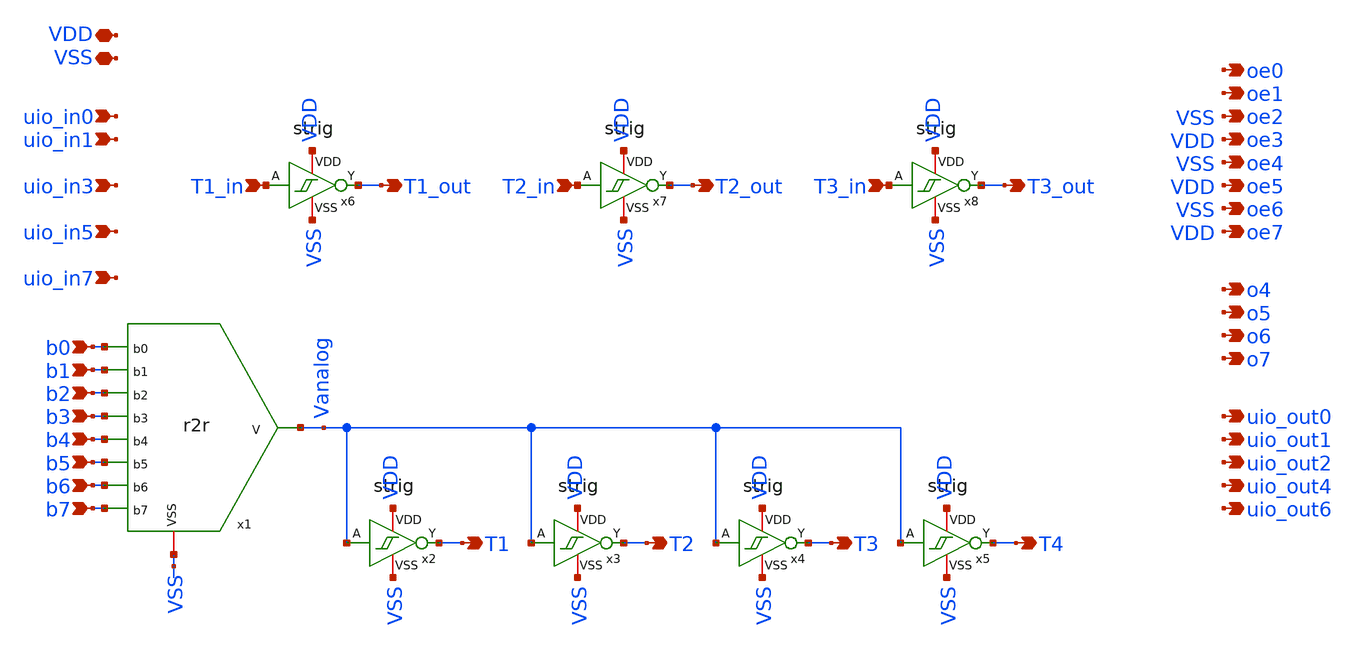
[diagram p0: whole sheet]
** sch_path: xschem/tt_um_mixer.sch
**.subckt tt_um_mixer b0 b1 b2 b3 b4 b5 b6 b7 VSS VDD T1 T2 T3 T4 T1_out T1_in T2_out T2_in T3_out
*+ T3_in oe0 oe1 oe2 oe3 oe4 oe5 oe6 oe7 uio_in0 uio_in1 uio_in3 uio_in5 uio_in7 o4 o5 o6 o7 uio_out0
*+ uio_out1 uio_out2 uio_out4 uio_out6
*.ipin b0
*.ipin b1
*.ipin b2
*.ipin b3
*.ipin b4
*.ipin b5
*.ipin b6
*.ipin b7
*.iopin VSS
*.iopin VDD
*.opin T1
*.opin T2
*.opin T3
*.opin T4
*.opin T1_out
*.ipin T1_in
*.opin T2_out
*.ipin T2_in
*.opin T3_out
*.ipin T3_in
*.opin oe0
*.opin oe1
*.opin oe2
*.opin oe3
*.opin oe4
*.opin oe5
*.opin oe6
*.opin oe7
*.ipin uio_in0
*.ipin uio_in1
*.ipin uio_in3
*.ipin uio_in5
*.ipin uio_in7
*.opin o4
*.opin o5
*.opin o6
*.opin o7
*.opin uio_out0
*.opin uio_out1
*.opin uio_out2
*.opin uio_out4
*.opin uio_out6
x2 VDD Vanalog T1 VSS strig WN1=.6u WN2=.6u WN3=.6u WP1=.6u WP2=.6u WP3=.6u
x1 b3 b1 b2 b0 b4 b5 b6 b7 Vanalog VSS r2r
x3 VDD Vanalog T2 VSS strig WN1=1.2u WN2=1.2u WN3=.6u WP1=1.2u WP2=1.2u WP3=.6u
x4 VDD Vanalog T3 VSS strig WN1=2.4u WN2=2.4u WN3=.6u WP1=2.4u WP2=2.4u WP3=.6u
x5 VDD Vanalog T4 VSS strig WN1=4.8u WN2=4.8u WN3=.6u WP1=4.8u WP2=4.8u WP3=.6u
x6 VDD T1_in T1_out VSS strig WN1=.6u WN2=.6u WN3=.6u WP1=.6u WP2=.6u WP3=.6u
x7 VDD T2_in T2_out VSS strig WN1=.6u WN2=.6u WN3=.6u WP1=.6u WP2=.6u WP3=.6u
x8 VDD T3_in T3_out VSS strig WN1=.6u WN2=.6u WN3=.6u WP1=.6u WP2=.6u WP3=.6u
**.ends

* expanding   symbol:  strig.sym # of pins=4
** sym_path: xschem/strig.sym
** sch_path: xschem/strig.sch
.subckt strig VDD A Y VSS  WN1=.15u WN2=.15u WN3=.15u WP1=.15u WP2=.15u WP3=.15u
*.iopin VDD
*.iopin VSS
*.ipin A
*.opin Y
XM1 net1 A VSS VSS sg13_lv_nmos w=WN1 l=0.13u ng=1 m=1 mm_ok=1
XM2 Y A net1 VSS sg13_lv_nmos w=WN2 l=0.13u ng=1 m=1 mm_ok=1
XM3 VDD Y net1 VSS sg13_lv_nmos w=WN3 l=0.13u ng=1 m=1 mm_ok=1
XM6 VSS Y net2 VDD sg13_lv_pmos w=WP3 l=0.13u ng=1 m=1 mm_ok=1
XM5 Y A net2 VDD sg13_lv_pmos w=WP2 l=0.13u ng=1 m=1 mm_ok=1
XM4 net2 A VDD VDD sg13_lv_pmos w=WP1 l=0.13u ng=1 m=1 mm_ok=1
.ends


* expanding   symbol:  r2r.sym # of pins=10
** sym_path: xschem/r2r.sym
** sch_path: xschem/r2r.sch
.subckt r2r b3 b1 b2 b0 b4 b5 b6 b7 V VSS
*.iopin VSS
*.ipin b0
*.ipin b1
*.ipin b2
*.ipin b3
*.ipin b4
*.ipin b5
*.ipin b6
*.ipin b7
*.opin V
XR1 net1 VSS sub! rsil w=.5u l=.5u m=1 mm_ok=1
XR2 b0 net1 sub! rsil w=.5u l=.5u m=1 mm_ok=1
XR3 net2 net1 sub! rsil w=1u l=.5u m=1 mm_ok=1
XR4 b1 net2 sub! rsil w=.5u l=.5u m=1 mm_ok=1
XR5 net3 net2 sub! rsil w=1u l=.5u m=1 mm_ok=1
XR6 b2 net3 sub! rsil w=.5u l=.5u m=1 mm_ok=1
XR7 net4 net3 sub! rsil w=1u l=.5u m=1 mm_ok=1
XR8 b3 net4 sub! rsil w=.5u l=.5u m=1 mm_ok=1
XR9 net5 net4 sub! rsil w=1u l=.5u m=1 mm_ok=1
XR10 b4 net5 sub! rsil w=.5u l=.5u m=1 mm_ok=1
XR11 net6 net5 sub! rsil w=1u l=.5u m=1 mm_ok=1
XR12 b5 net6 sub! rsil w=.5u l=.5u m=1 mm_ok=1
XR13 net7 net6 sub! rsil w=1u l=.5u m=1 mm_ok=1
XR14 b6 net7 sub! rsil w=.5u l=.5u m=1 mm_ok=1
XR15 net8 net7 sub! rsil w=1u l=.5u m=1 mm_ok=1
XR16 b7 net8 sub! rsil w=.5u l=.5u m=1 mm_ok=1
XR17 V net8 sub! rsil w=1u l=.5u m=1 mm_ok=1
.ends

.end
